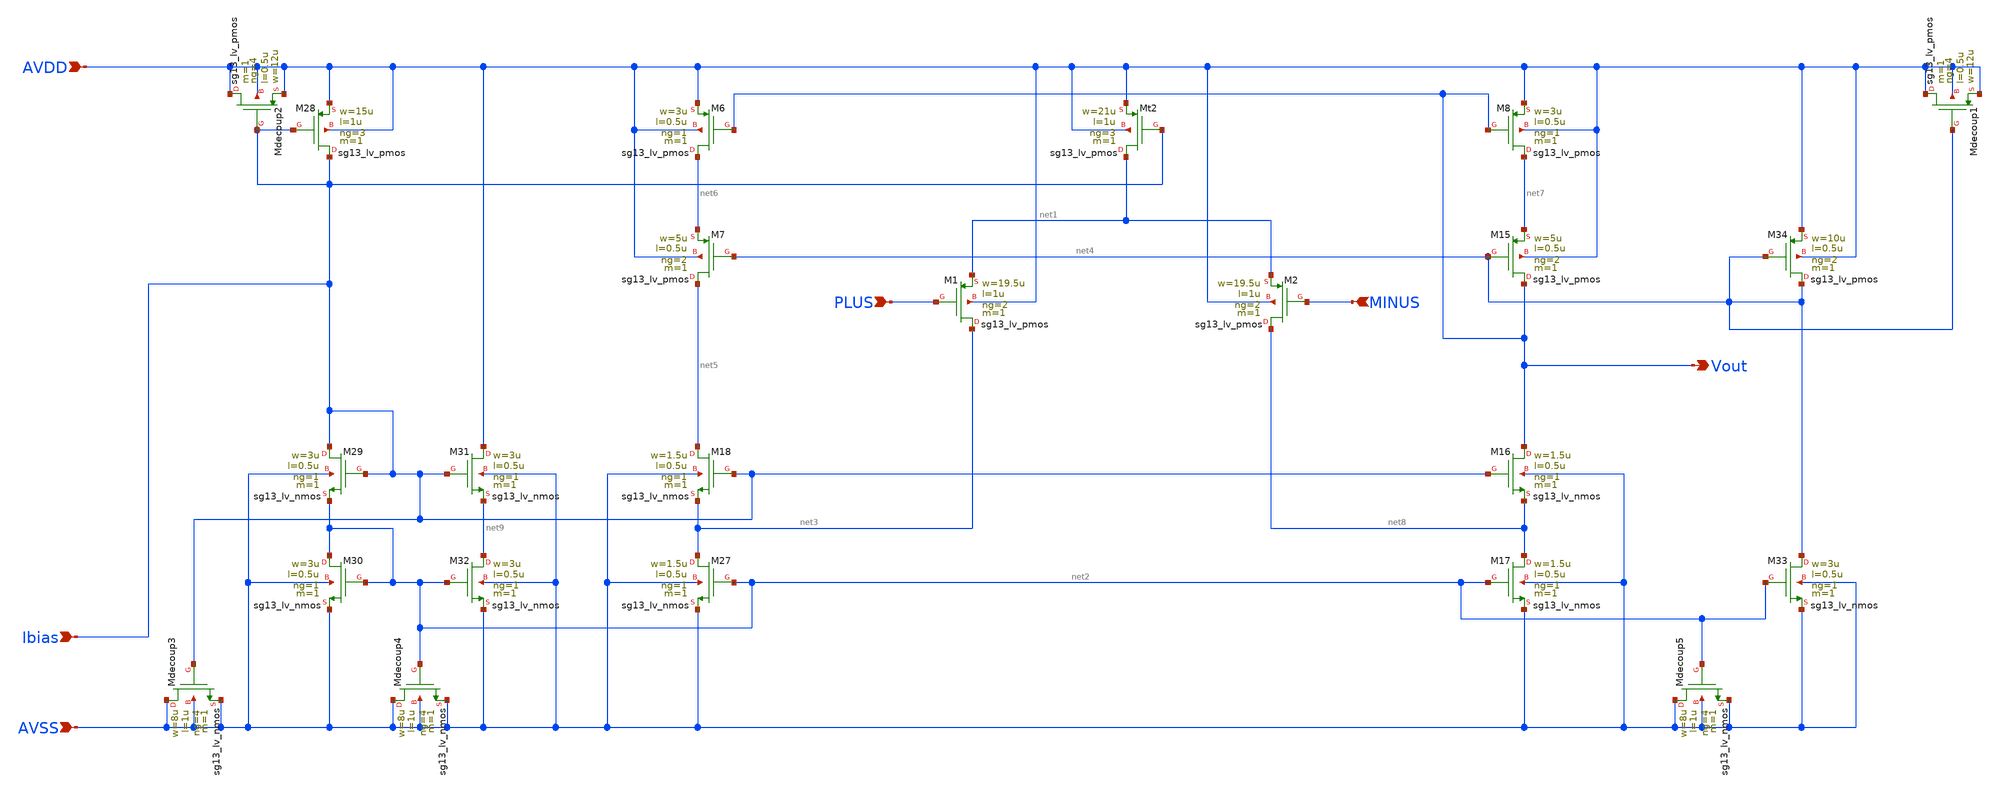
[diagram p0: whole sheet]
** sch_path: Designs/otas/foldedcascode.sch
* (c) 2025 Thesis_HP, Apache-2.0 license
**.subckt foldedcascode AVDD AVSS PLUS MINUS Vout Ibias
*.ipin AVDD
*.ipin AVSS
*.ipin PLUS
*.ipin MINUS
*.opin Vout
*.ipin Ibias
XMt2 net1 Ibias AVDD AVDD sg13_lv_pmos w=21u l=1u ng=3 m=1 mm_ok=1
XM1 net3 PLUS net1 AVDD sg13_lv_pmos w=19.5u l=1u ng=2 m=1 mm_ok=1
XM2 net8 MINUS net1 AVDD sg13_lv_pmos w=19.5u l=1u ng=2 m=1 mm_ok=1
XM6 net6 Vout AVDD AVDD sg13_lv_pmos w=3u l=0.5u ng=1 m=1 mm_ok=1
XM7 net5 net4 net6 AVDD sg13_lv_pmos w=5u l=0.5u ng=2 m=1 mm_ok=1
XM8 net7 Vout AVDD AVDD sg13_lv_pmos w=3u l=0.5u ng=1 m=1 mm_ok=1
XM15 Vout net4 net7 AVDD sg13_lv_pmos w=5u l=0.5u ng=2 m=1 mm_ok=1
XM16 Vout Ibias net8 AVSS sg13_lv_nmos w=1.5u l=0.5u ng=1 m=1 mm_ok=1
XM17 net8 net2 AVSS AVSS sg13_lv_nmos w=1.5u l=0.5u ng=1 m=1 mm_ok=1
XM18 net5 Ibias net3 AVSS sg13_lv_nmos w=1.5u l=0.5u ng=1 m=1 mm_ok=1
XM27 net3 net2 AVSS AVSS sg13_lv_nmos w=1.5u l=0.5u ng=1 m=1 mm_ok=1
XM28 Ibias Ibias AVDD AVDD sg13_lv_pmos w=15u l=1u ng=3 m=1 mm_ok=1
XM29 Ibias Ibias net2 AVSS sg13_lv_nmos w=3u l=0.5u ng=1 m=1 mm_ok=1
XM30 net2 net2 AVSS AVSS sg13_lv_nmos w=3u l=0.5u ng=1 m=1 mm_ok=1
XM31 AVDD Ibias net9 AVSS sg13_lv_nmos w=3u l=0.5u ng=1 m=1 mm_ok=1
XM32 net9 net2 AVSS AVSS sg13_lv_nmos w=3u l=0.5u ng=1 m=1 mm_ok=1
XM33 net4 net2 AVSS AVSS sg13_lv_nmos w=3u l=0.5u ng=1 m=1 mm_ok=1
XM34 net4 net4 AVDD AVDD sg13_lv_pmos w=10u l=0.5u ng=2 m=1 mm_ok=1
XMdecoup1 AVDD net4 AVDD AVDD sg13_lv_pmos w=12u l=0.5u ng=4 m=1 mm_ok=1
XMdecoup2 AVDD Ibias AVDD AVDD sg13_lv_pmos w=12u l=0.5u ng=4 m=1 mm_ok=1
XMdecoup3 AVSS Ibias AVSS AVSS sg13_lv_nmos w=8u l=1u ng=4 m=1 mm_ok=1
XMdecoup4 AVSS net2 AVSS AVSS sg13_lv_nmos w=8u l=1u ng=4 m=1 mm_ok=1
XMdecoup5 AVSS net2 AVSS AVSS sg13_lv_nmos w=8u l=1u ng=4 m=1 mm_ok=1
**.ends
.end
